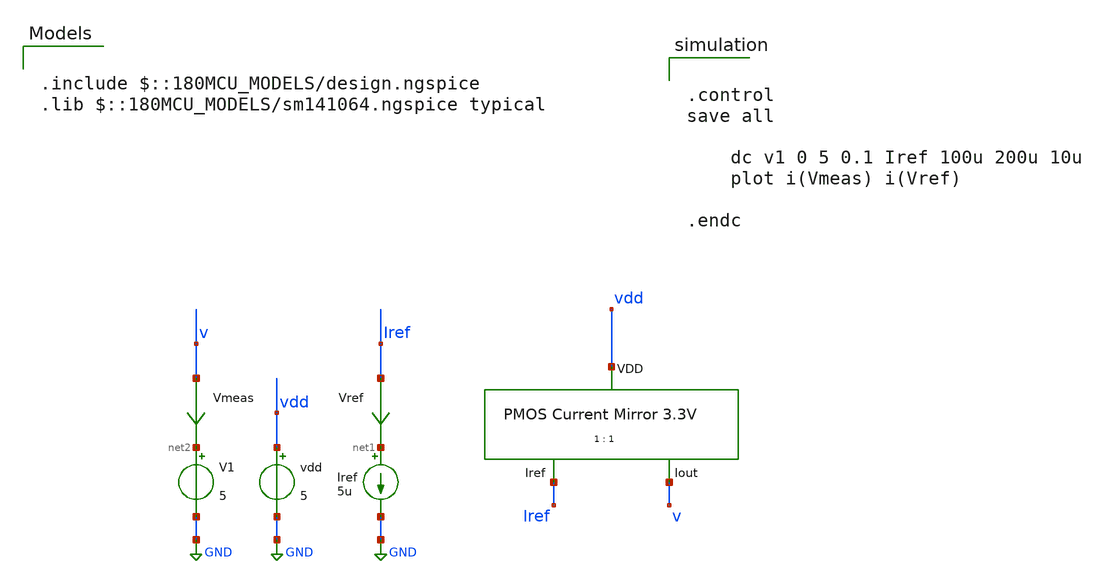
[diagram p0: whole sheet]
** sch_path: designs/libs/tb_analog/tb_pmos_current_mirror/tb_pmos_current_mirror.sch
**.subckt tb_pmos_current_mirror
Iref net1 GND 5u
vdd vdd GND 5
V1 net2 GND 5
Vmeas v net2 0
.save i(vmeas)
Vref Iref net1 0
.save i(vref)
x1 vdd v Iref pmos_current_mirror
**** begin user architecture code


.control
save all

	dc v1 0 5 0.1 Iref 100u 200u 10u
	plot i(Vmeas) i(Vref)

.endc



.include $::180MCU_MODELS/design.ngspice
.lib $::180MCU_MODELS/sm141064.ngspice typical

**** end user architecture code
**.ends

* expanding   symbol:  libs/core_analog/pmos_current_mirror/pmos_current_mirror.sym # of pins=3
** sym_path: designs/libs/core_analog/pmos_current_mirror/pmos_current_mirror.sym
** sch_path: designs/libs/core_analog/pmos_current_mirror/pmos_current_mirror.sch
.subckt pmos_current_mirror VDD Iout Iref
*.ipin VDD
*.ipin Iref
*.opin Iout
XM2 net1 net1 VDD VDD pfet_06v0 L=5u W=11u nf=1 ad='int((nf+1)/2) * W/nf * 0.18u' as='int((nf+2)/2) * W/nf * 0.18u'
+ pd='2*int((nf+1)/2) * (W/nf + 0.18u)' ps='2*int((nf+2)/2) * (W/nf + 0.18u)' nrd='0.18u / W' nrs='0.18u / W'
+ sa=0 sb=0 sd=0 m=1
XM1 net2 net1 VDD VDD pfet_06v0 L=5u W=11u nf=1 ad='int((nf+1)/2) * W/nf * 0.18u' as='int((nf+2)/2) * W/nf * 0.18u'
+ pd='2*int((nf+1)/2) * (W/nf + 0.18u)' ps='2*int((nf+2)/2) * (W/nf + 0.18u)' nrd='0.18u / W' nrs='0.18u / W'
+ sa=0 sb=0 sd=0 m=1
XM3 Iref Iref net1 net1 pfet_06v0 L=5u W=11u nf=1 ad='int((nf+1)/2) * W/nf * 0.18u' as='int((nf+2)/2) * W/nf * 0.18u'
+ pd='2*int((nf+1)/2) * (W/nf + 0.18u)' ps='2*int((nf+2)/2) * (W/nf + 0.18u)' nrd='0.18u / W' nrs='0.18u / W'
+ sa=0 sb=0 sd=0 m=1
XM4 Iout Iref net2 net2 pfet_06v0 L=5u W=11u nf=1 ad='int((nf+1)/2) * W/nf * 0.18u' as='int((nf+2)/2) * W/nf * 0.18u'
+ pd='2*int((nf+1)/2) * (W/nf + 0.18u)' ps='2*int((nf+2)/2) * (W/nf + 0.18u)' nrd='0.18u / W' nrs='0.18u / W'
+ sa=0 sb=0 sd=0 m=1
.ends

.GLOBAL GND
.end
